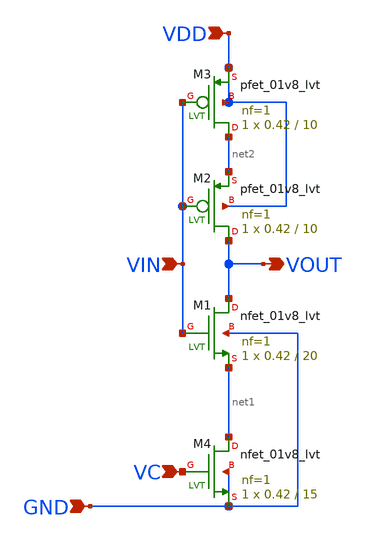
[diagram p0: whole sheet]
** sch_path: design/LELO_SVOD_SKY130A/LELO_RING_DEL_VC.sch
**.subckt LELO_RING_DEL_VC VIN VDD GND VOUT VC
*.ipin VIN
*.ipin VDD
*.ipin GND
*.opin VOUT
*.ipin VC
XM1 VOUT VIN net1 GND sky130_fd_pr__nfet_01v8_lvt L=20 W=0.42 nf=1 ad='int((1 + 1)/2) * 0.42 / 1 * 0.29'
+ as='int((1 + 2)/2) * 0.42 / 1 * 0.29' pd='2*int((1 + 1)/2) * (0.42 / 1 + 0.29)' ps='2*int((1 + 2)/2) * (0.42 / 1 + 0.29)'
+ nrd='0.29 / 0.42 ' nrs='0.29 / 0.42 ' sa=0 sb=0 sd=0 mult=1 m=1
XM2 VOUT VIN net2 VDD sky130_fd_pr__pfet_01v8_lvt L=10 W=0.42 nf=1 ad='int((1 + 1)/2) * 0.42 / 1 * 0.29'
+ as='int((1 + 2)/2) * 0.42 / 1 * 0.29' pd='2*int((1 + 1)/2) * (0.42 / 1 + 0.29)' ps='2*int((1 + 2)/2) * (0.42 / 1 + 0.29)'
+ nrd='0.29 / 0.42 ' nrs='0.29 / 0.42 ' sa=0 sb=0 sd=0 mult=1 m=1
XM4 net1 VC GND GND sky130_fd_pr__nfet_01v8_lvt L=15 W=0.42 nf=1 ad='int((1 + 1)/2) * 0.42 / 1 * 0.29'
+ as='int((1 + 2)/2) * 0.42 / 1 * 0.29' pd='2*int((1 + 1)/2) * (0.42 / 1 + 0.29)' ps='2*int((1 + 2)/2) * (0.42 / 1 + 0.29)'
+ nrd='0.29 / 0.42 ' nrs='0.29 / 0.42 ' sa=0 sb=0 sd=0 mult=1 m=1
XM3 net2 VIN VDD VDD sky130_fd_pr__pfet_01v8_lvt L=10 W=0.42 nf=1 ad='int((1 + 1)/2) * 0.42 / 1 * 0.29'
+ as='int((1 + 2)/2) * 0.42 / 1 * 0.29' pd='2*int((1 + 1)/2) * (0.42 / 1 + 0.29)' ps='2*int((1 + 2)/2) * (0.42 / 1 + 0.29)'
+ nrd='0.29 / 0.42 ' nrs='0.29 / 0.42 ' sa=0 sb=0 sd=0 mult=1 m=1
**.ends
.end
